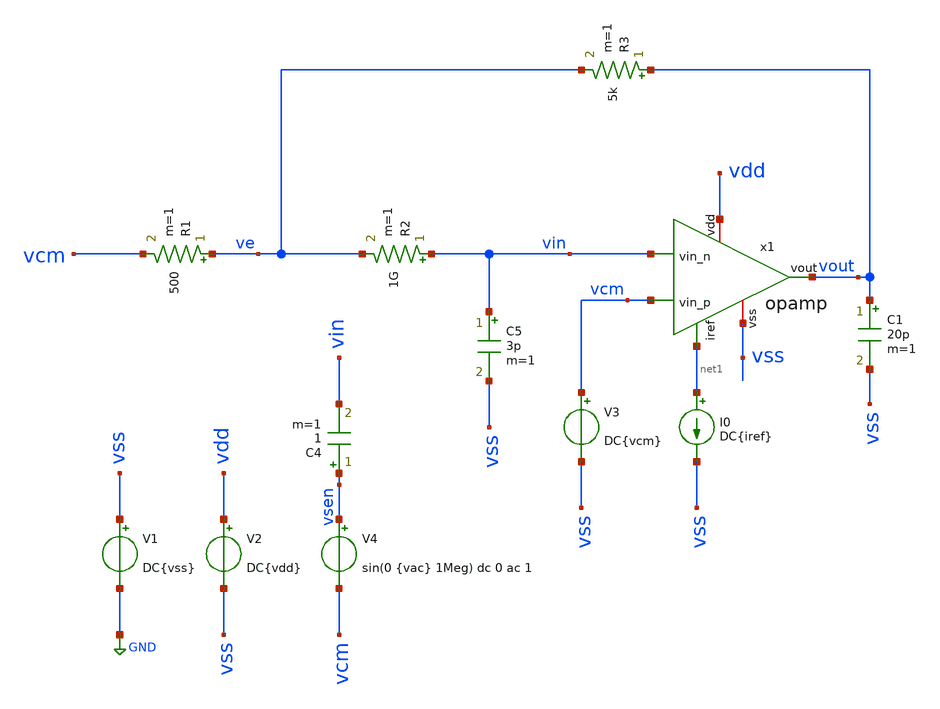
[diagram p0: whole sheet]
** sch_path: tb_opamp_openloop.sch
**.subckt tb_opamp_openloop
V1 vss GND DC{vss}
V2 vdd vss DC{vdd}
V3 vcm vss DC{vcm}
V4 vsen vcm sin(0 {vac} 1Meg) dc 0 ac 1
C4 vsen vin 1 m=1
I0 net1 vss DC{iref}
R1 ve vcm 500 m=1
R2 vin ve 1G m=1
R3 vout ve 5k m=1
C5 vin vss 3p m=1
C1 vout vss 20p m=1
x1 vdd net1 vin vcm vout vss opamp
**** begin user architecture code




* Circuit Parameters
.param iref = 100u
.param vdd  = 1.8
.param vss  = 0.0
.param vcm  = vdd/2
.param vac  = 60m

.param mul8 = 2
.param mul5 = 20
.param mul7 = 150
.param w857 = 70
.param l857 = 7

.param l34  = 3
.param w34  = 60
.param mul34 = 2

.param mpar = 333
.param lpar = 0.5
.param wpar = 10

.param mul6 = 90
.param l6   = 0.15
.param w6   = 25

.param mul9 = 1
.param l9   = 0.15
.param w9   = 10

.param res_1 = 333
.param cap_1 = 5p

.options TEMP = 65

* Include Models
.lib ~/skywater/skywater-pdk/libraries/sky130_fd_pr_ngspice/latest/models/corners/sky130.lib TT

* OP Parameters & Singals to save
.save all  @M.X1.XM9.msky130_fd_pr__nfet_01v8[gds]  @M.X1.XM1.msky130_fd_pr__pfet_01v8_lvt[id] @M.X1.XM1.msky130_fd_pr__pfet_01v8_lvt[vth] @M.X1.XM1.msky130_fd_pr__pfet_01v8_lvt[vgs] @M.X1.XM1.msky130_fd_pr__pfet_01v8_lvt[vds] @M.X1.XM1.msky130_fd_pr__pfet_01v8_lvt[vdsat] @M.X1.XM1.msky130_fd_pr__pfet_01v8_lvt[gm] @M.X1.XM1.msky130_fd_pr__pfet_01v8_lvt[gds]  @M.X1.XM2.msky130_fd_pr__pfet_01v8_lvt[id] @M.X1.XM2.msky130_fd_pr__pfet_01v8_lvt[vth] @M.X1.XM2.msky130_fd_pr__pfet_01v8_lvt[vgs] @M.X1.XM2.msky130_fd_pr__pfet_01v8_lvt[vds] @M.X1.XM2.msky130_fd_pr__pfet_01v8_lvt[vdsat] @M.X1.XM2.msky130_fd_pr__pfet_01v8_lvt[gm] @M.X1.XM2.msky130_fd_pr__pfet_01v8_lvt[gds]  @M.X1.XM3.msky130_fd_pr__nfet_01v8[id] @M.X1.XM3.msky130_fd_pr__nfet_01v8[vth] @M.X1.XM3.msky130_fd_pr__nfet_01v8[vgs] @M.X1.XM3.msky130_fd_pr__nfet_01v8[vds] @M.X1.XM3.msky130_fd_pr__nfet_01v8[vdsat] @M.X1.XM3.msky130_fd_pr__nfet_01v8[gm] @M.X1.XM3.msky130_fd_pr__nfet_01v8[gds]  @M.X1.XM4.msky130_fd_pr__nfet_01v8[id] @M.X1.XM4.msky130_fd_pr__nfet_01v8[vth] @M.X1.XM4.msky130_fd_pr__nfet_01v8[vgs] @M.X1.XM4.msky130_fd_pr__nfet_01v8[vds] @M.X1.XM4.msky130_fd_pr__nfet_01v8[vdsat] @M.X1.XM4.msky130_fd_pr__nfet_01v8[gm] @M.X1.XM4.msky130_fd_pr__nfet_01v8[gds]  @M.X1.XM5.msky130_fd_pr__pfet_01v8[id] @M.X1.XM5.msky130_fd_pr__pfet_01v8[vth] @M.X1.XM5.msky130_fd_pr__pfet_01v8[vgs] @M.X1.XM5.msky130_fd_pr__pfet_01v8[vds] @M.X1.XM5.msky130_fd_pr__pfet_01v8[vdsat] @M.X1.XM5.msky130_fd_pr__pfet_01v8[gm] @M.X1.XM5.msky130_fd_pr__pfet_01v8[gds]  @M.X1.XM6.msky130_fd_pr__nfet_01v8[id] @M.X1.XM6.msky130_fd_pr__nfet_01v8[vth] @M.X1.XM6.msky130_fd_pr__nfet_01v8[vgs] @M.X1.XM6.msky130_fd_pr__nfet_01v8[vds] @M.X1.XM6.msky130_fd_pr__nfet_01v8[vdsat] @M.X1.XM6.msky130_fd_pr__nfet_01v8[gm] @M.X1.XM6.msky130_fd_pr__nfet_01v8[gds]   @M.X1.XM7.msky130_fd_pr__pfet_01v8[id] @M.X1.XM7.msky130_fd_pr__pfet_01v8[vth] @M.X1.XM7.msky130_fd_pr__pfet_01v8[vgs] @M.X1.XM7.msky130_fd_pr__pfet_01v8[vds] @M.X1.XM7.msky130_fd_pr__pfet_01v8[vdsat] @M.X1.XM7.msky130_fd_pr__pfet_01v8[gm] @M.X1.XM7.msky130_fd_pr__pfet_01v8[gds]   @M.X1.XM6.msky130_fd_pr__nfet_01v8[cgg]  @M.X1.XM8.msky130_fd_pr__pfet_01v8[id] @M.X1.XM8.msky130_fd_pr__pfet_01v8[vth] @M.X1.XM8.msky130_fd_pr__pfet_01v8[vgs] @M.X1.XM8.msky130_fd_pr__pfet_01v8[vds] @M.X1.XM8.msky130_fd_pr__pfet_01v8[vdsat] @M.X1.XM8.msky130_fd_pr__pfet_01v8[gm] @M.X1.XM8.msky130_fd_pr__pfet_01v8[gds]  @M.X1.XM9.msky130_fd_pr__nfet_01v8[id] @M.X1.XM9.msky130_fd_pr__nfet_01v8[vth] @M.X1.XM9.msky130_fd_pr__nfet_01v8[vgs] @M.X1.XM9.msky130_fd_pr__nfet_01v8[vds] @M.X1.XM9.msky130_fd_pr__nfet_01v8[vdsat] @M.X1.XM9.msky130_fd_pr__nfet_01v8[gm] @M.X1.XM9.msky130_fd_pr__nfet_01v8[gds] @M.X1.XM1.msky130_fd_pr__nfet_01v8[vdsat] @M.X1.XM2.msky130_fd_pr__nfet_01v8[vdsat] @M.X1.XM3.msky130_fd_pr__nfet_01v8[vdsat] @M.X1.XM4.msky130_fd_pr__nfet_01v8[vdsat] @M.X1.XM5.msky130_fd_pr__nfet_01v8[vdsat] @M.X1.XM6.msky130_fd_pr__nfet_01v8[vdsat] @M.X1.XM7.msky130_fd_pr__nfet_01v8[vdsat] @M.X1.XM8.msky130_fd_pr__nfet_01v8[vdsat] @M.X1.XM9.msky130_fd_pr__nfet_01v8[vdsat]
*Simulation
.control

  ac dec 100 1 10G
  setplot ac1
  meas ac GBW when vdb(vout)=0
  meas ac DCG find vdb(vout) at=1
  meas ac PM find vp(vout) when vdb(vout)=0
  print PM*180/PI
  meas ac GM find vdb(vout) when vp(vout)=0
  plot vdb(vout) {vp(vout)*180/PI}
  write tb_opamp_openloop_ac1.raw

  reset
  op
  setplot op1
  unset filetype
  write tb_opamp_openloop.raw

.endc
.probe I(x1,vdd)
.end


**** end user architecture code
**.ends

* expanding   symbol:  opamp.sym # of pins=6
** sym_path: opamp.sym
** sch_path: opamp.sch
.subckt opamp vdd iref vin_n vin_p vout vss
*.iopin vdd
*.iopin vss
*.ipin vin_n
*.ipin vin_p
*.ipin iref
*.opin vout
XM3 vbn vbn vss vss sky130_fd_pr__nfet_01v8 L={L34} W={W34} nf=1 ad='W * 0.29' as='W * 0.29' pd='2 * (W + 0.29)'
+ ps='2 * (W + 0.29)' nrd='0.29 / W' nrs='0.29 / W' sa=0 sb=0 sd=0 mult={mul34} m={mul34}
XM4 voe1 vbn vss vss sky130_fd_pr__nfet_01v8 L={L34} W={W34} nf=1 ad='W * 0.29' as='W * 0.29' pd='2 * (W + 0.29)'
+ ps='2 * (W + 0.29)' nrd='0.29 / W' nrs='0.29 / W' sa=0 sb=0 sd=0 mult={mul34} m={mul34}
XM5 vp iref vdd vdd sky130_fd_pr__pfet_01v8 L={L857} W={W857} nf=1 ad='W * 0.29' as='W * 0.29' pd='2 * (W + 0.29)'
+ ps='2 * (W + 0.29)' nrd='0.29 / W' nrs='0.29 / W' sa=0 sb=0 sd=0 mult={mul5} m={mul5}
XM7 vout iref vdd vdd sky130_fd_pr__pfet_01v8 L={L857} W={W857} nf=1 ad='W * 0.29' as='W * 0.29' pd='2 * (W + 0.29)'
+ ps='2 * (W + 0.29)' nrd='0.29 / W' nrs='0.29 / W' sa=0 sb=0 sd=0 mult={mul7} m={mul7}
XM8 iref iref vdd vdd sky130_fd_pr__pfet_01v8 L={L857} W={W857} nf=1 ad='W * 0.29' as='W * 0.29' pd='2 * (W + 0.29)'
+ ps='2 * (W + 0.29)' nrd='0.29 / W' nrs='0.29 / W' sa=0 sb=0 sd=0 mult={mul8} m={mul8}
XM9 net1 vdd voe1 vss sky130_fd_pr__nfet_01v8 L={l9} W={w9} nf=1 ad='W * 0.29' as='W * 0.29' pd='2 * (W + 0.29)'
+ ps='2 * (W + 0.29)' nrd='0.29 / W' nrs='0.29 / W' sa=0 sb=0 sd=0 mult={mul9} m={mul9}
XM6 vout voe1 vss vss sky130_fd_pr__nfet_01v8 L={l6} W={w6} nf=1 ad='W * 0.29' as='W * 0.29' pd='2 * (W + 0.29)'
+ ps='2 * (W + 0.29)' nrd='0.29 / W' nrs='0.29 / W' sa=0 sb=0 sd=0 mult={mul6} m={mul6}
XM1 vbn vin_n vp vp sky130_fd_pr__pfet_01v8_lvt L={lpar} W={wpar} nf=1 ad='int((nf+1)/2) * W/nf * 0.29'
+ as='int((nf+2)/2) * W/nf * 0.29' pd='2*int((nf+1)/2) * (W/nf + 0.29)' ps='2*int((nf+2)/2) * (W/nf + 0.29)'
+ nrd='0.29 / W' nrs='0.29 / W' sa=0 sb=0 sd=0 mult={mpar} m={mpar}
XM2 voe1 vin_p vp vp sky130_fd_pr__pfet_01v8_lvt L={lpar} W={wpar} nf=1 ad='int((nf+1)/2) * W/nf * 0.29'
+ as='int((nf+2)/2) * W/nf * 0.29' pd='2*int((nf+1)/2) * (W/nf + 0.29)' ps='2*int((nf+2)/2) * (W/nf + 0.29)'
+ nrd='0.29 / W' nrs='0.29 / W' sa=0 sb=0 sd=0 mult={mpar} m={mpar}
C1 net1 vout {cap_1} m=1
R1 vdd vdd {res_1} m=1
.ends

.GLOBAL GND
.end
